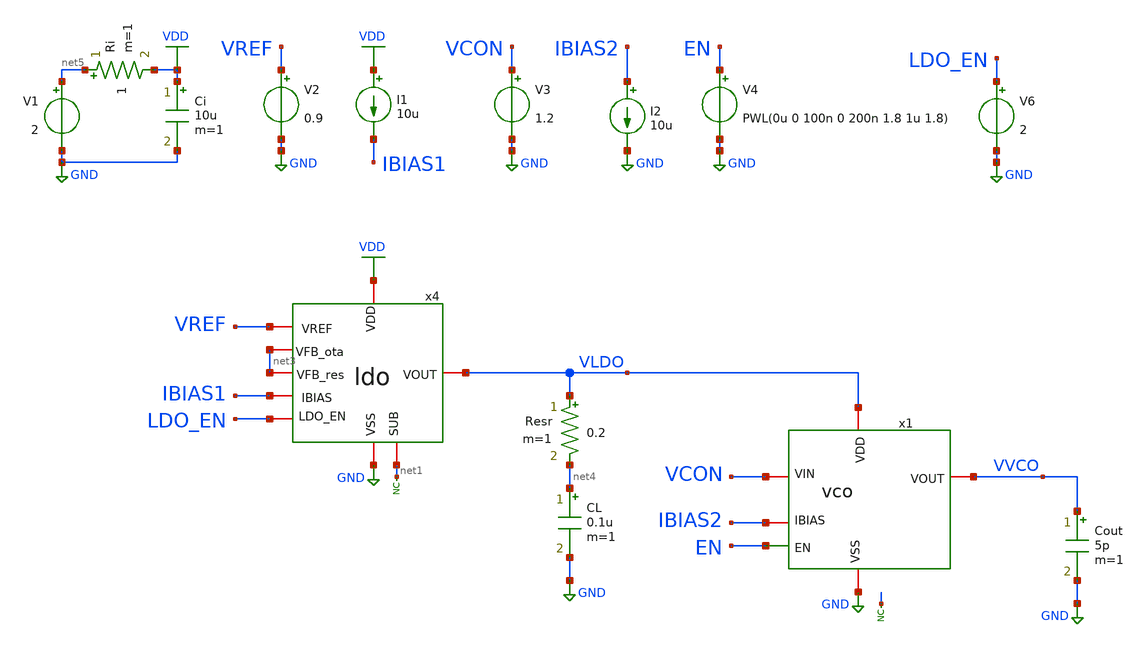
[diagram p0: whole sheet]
** sch_path: designs/libs/A1_tb/tb_top_ldo_vco/tb_top_ldo_vco.sch
**.subckt tb_top_ldo_vco
V3 VCON GND 1.2
I2 IBIAS2 GND 10u
V4 EN GND PWL(0u 0 100n 0 200n 1.8 1u 1.8)
x1 VLDO IBIAS2 VVCO EN GND VCON vco
x4 VDD VREF VLDO IBIAS1 net1 GND LDO_EN net3 net3 ldo
* noconn #net1
* noconn #net2
V2 VREF GND 0.9
CL net4 GND 0.1u m=1
Resr VLDO net4 0.2 m=1
I1 VDD IBIAS1 10u
Ri net5 VDD 1 m=1
Ci VDD GND 10u m=1
V1 net5 GND 2
Cout VVCO GND 5p m=1
V6 LDO_EN GND 2
**** begin user architecture code



.control
save all

run
set color0 = white

** Simulations Temperature and Line Regulation
dc TEMP -40 125 1  V1 2 5 0.05

** Measurements
meas dc Vldo_max MAX v(VLDO)
meas dc Vldo_min MIN v(VLDO)
let dev_max = abs(Vldo_max - 1.8)
print dev_max
let dev_min = abs(Vldo_min - 1.8)
print dev_min
let Vldo_acc_abs = max(dev_max, dev_min)
print Vldo_acc_abs
let Vldo_acc_rel = (Vldo_acc_abs / 1.8) * 100
print Vldo_acc_rel

** Plots
setplot dc1
let vldo=v(VLDO)
plot vldo



write tb_top_ldo_vco.raw

.endc
* ngspice commands




.include $::180MCU_MODELS/design.ngspice
.lib $::180MCU_MODELS/sm141064.ngspice typical
.lib $::180MCU_MODELS/sm141064.ngspice cap_mim
.lib $::180MCU_MODELS/sm141064.ngspice moscap_typical
.lib $::180MCU_MODELS/sm141064.ngspice mimcap_typical
.lib $::180MCU_MODELS/sm141064.ngspice res_typical
* .lib $::180MCU_MODELS/sm141064.ngspice res_statistical
* ngspice commands

**** end user architecture code
**.ends
.GLOBAL GND
.GLOBAL VDD
.end
